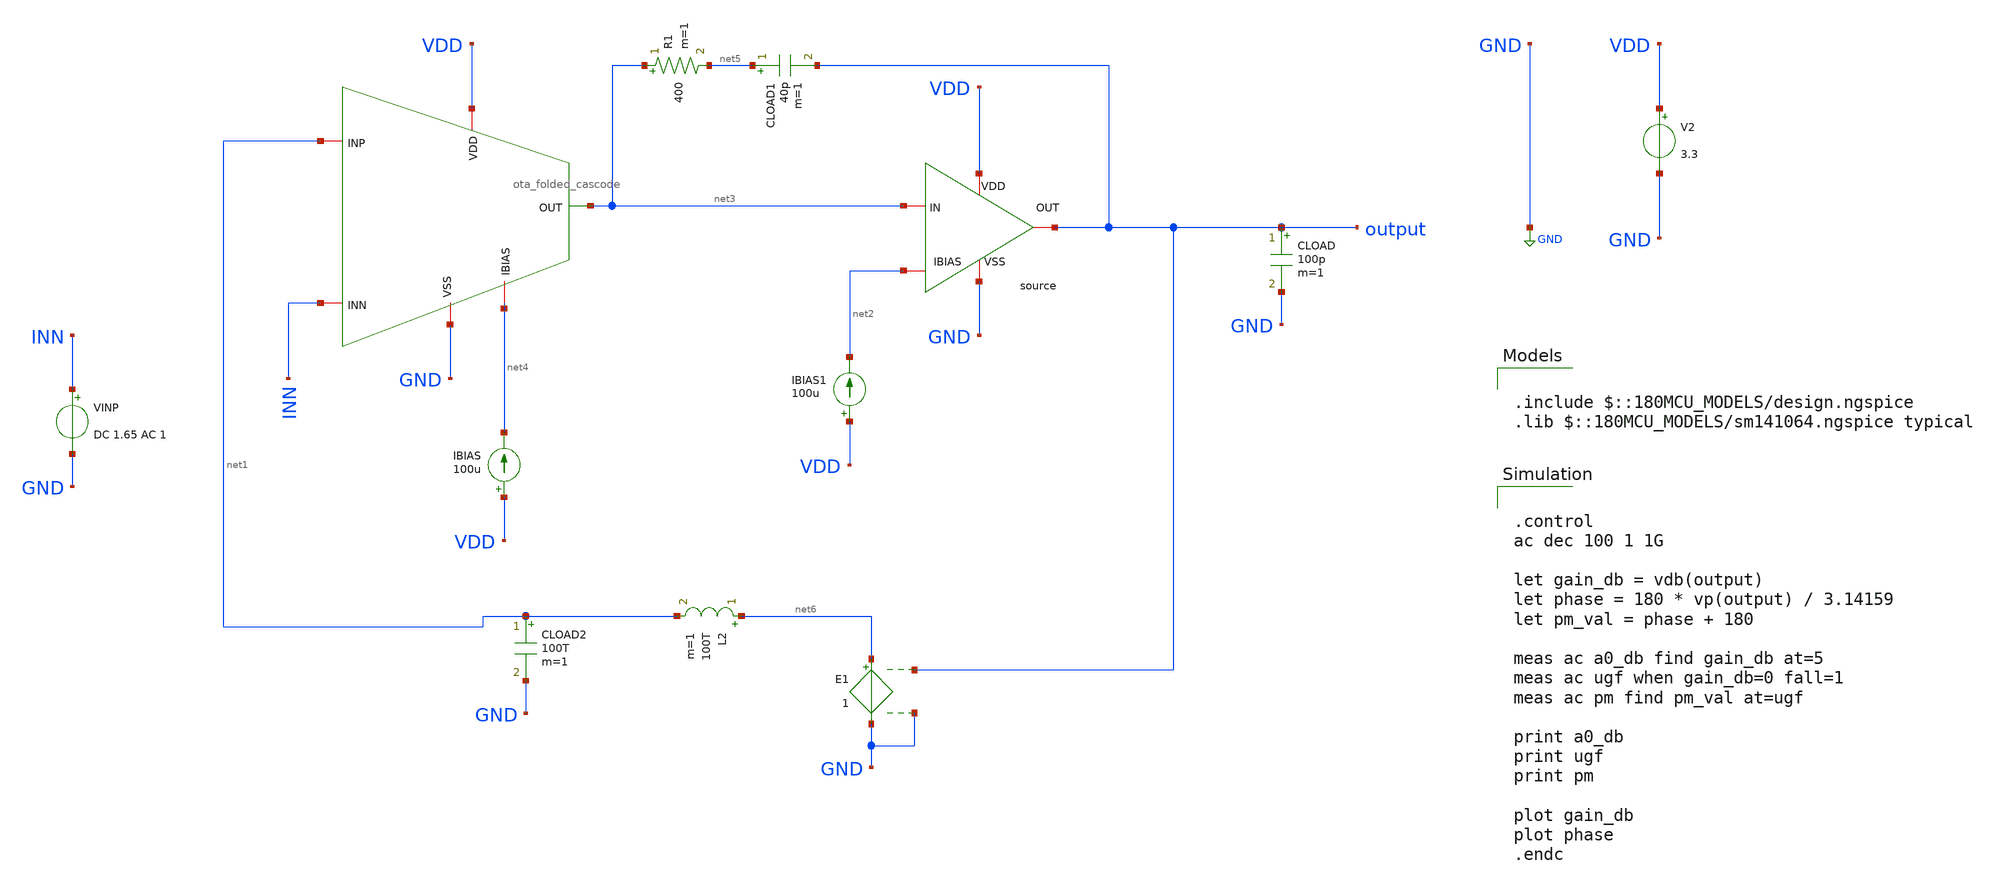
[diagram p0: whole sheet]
** sch_path: designs/libs/core_amps/two_stage_amps/folded_cs_ac_tb.sch
**.subckt folded_cs_ac_tb
x1 VDD GND net3 net1 INN net4 ota_folded_cascode
x2 VDD net3 net2 output GND cs_schematic
V2 VDD GND 3.3
IBIAS VDD net4 100u
IBIAS1 VDD net2 100u
CLOAD output GND 100p m=1
CLOAD1 net5 output 40p m=1
R1 net3 net5 400 m=1
VINP INN GND DC 1.65 AC 1
L2 net6 net1 100T m=1
CLOAD2 net1 GND 100T m=1
E1 net6 GND output GND 1
**** begin user architecture code

.include $::180MCU_MODELS/design.ngspice
.lib $::180MCU_MODELS/sm141064.ngspice typical



.control
ac dec 100 1 1G

let gain_db = vdb(output)
let phase = 180 * vp(output) / 3.14159
let pm_val = phase + 180

meas ac a0_db find gain_db at=5
meas ac ugf when gain_db=0 fall=1
meas ac pm find pm_val at=ugf

print a0_db
print ugf
print pm

plot gain_db
plot phase
.endc


**** end user architecture code
**.ends
.GLOBAL GND
.end
